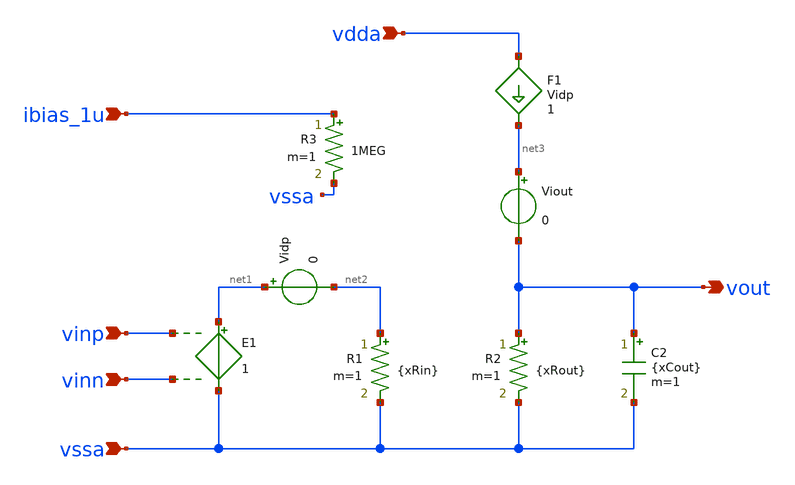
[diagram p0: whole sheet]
** sch_path: Running_vloga_in_ngspice/OTA_ideal_order1_elmod.sch
**.subckt OTA_ideal_order1_elmod vssa vinp ibias_1u vinn vdda vout
*.ipin vssa
*.ipin vinp
*.ipin ibias_1u
*.ipin vinn
*.ipin vdda
*.opin vout
E1 net1 vssa vinp vinn 1
R1 net2 vssa {xRin} m=1
F1 vdda net3 Vidp 1
Vidp net1 net2 0
R2 vout vssa {xRout} m=1
C2 vout vssa {xCout} m=1
Viout net3 vout 0
R3 ibias_1u vssa 1MEG m=1
**.ends
.end
